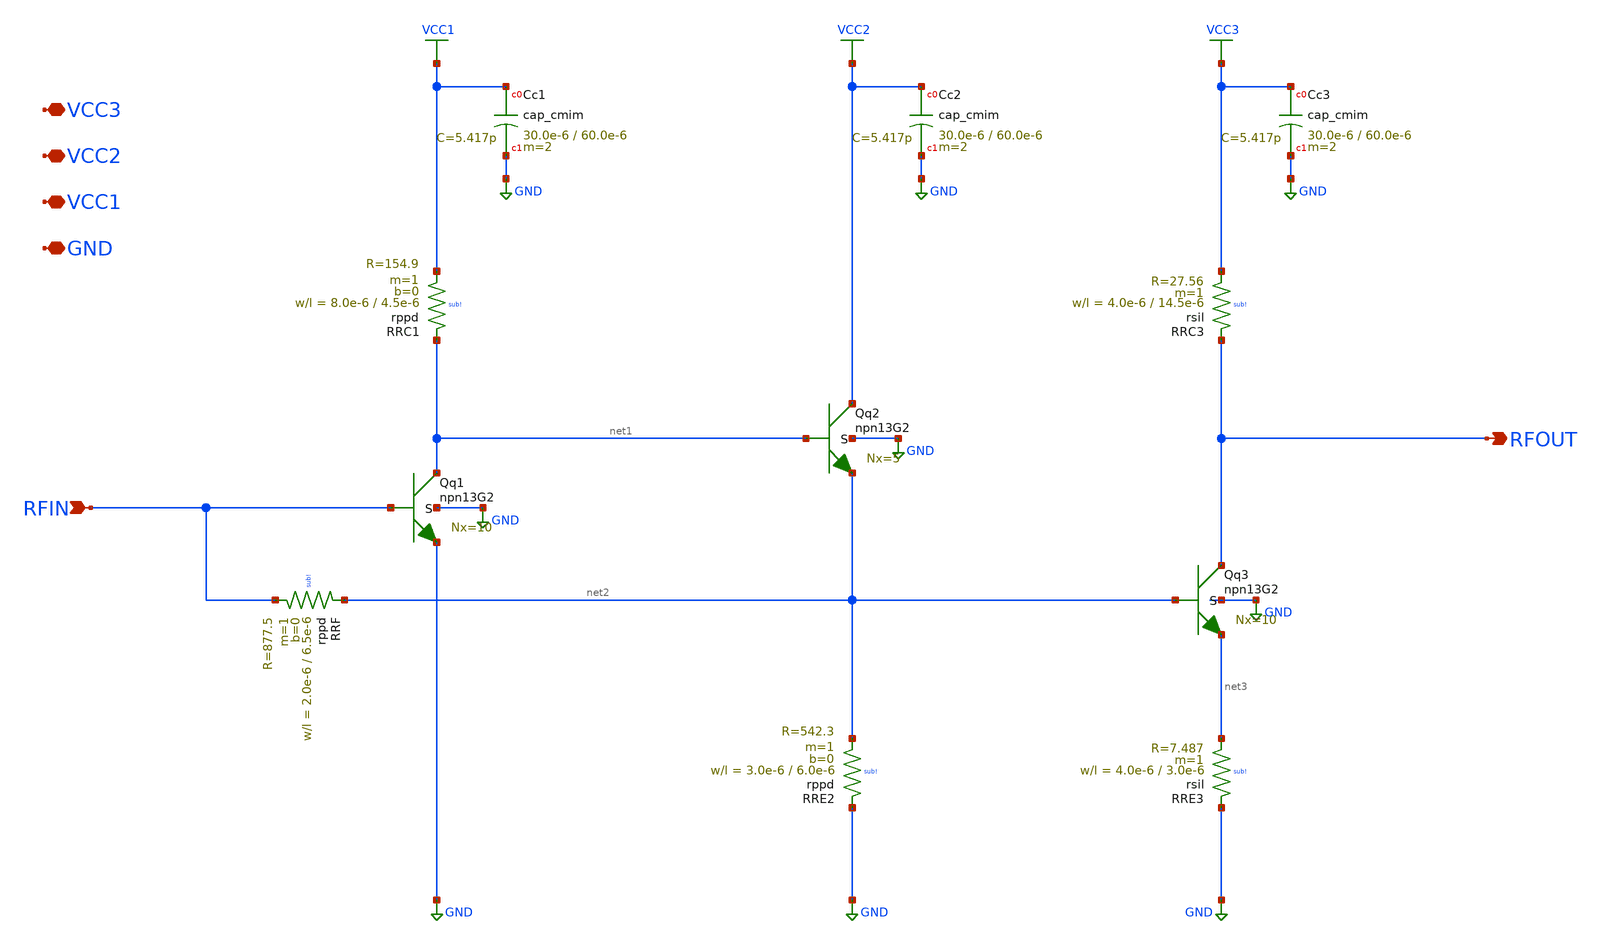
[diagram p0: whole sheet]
** sch_path: TO_Apr2025/40_GHZ_LOW_NOISE_TIA/xschem/40_GHZ_LOW_NOISE_TIA.sch
**.subckt 40_GHZ_LOW_NOISE_TIA RFIN GND VCC1 VCC2 RFOUT VCC3
*.ipin RFIN
*.iopin GND
*.iopin VCC1
*.iopin VCC2
*.opin RFOUT
*.iopin VCC3
XQq1 net1 RFIN GND GND npn13G2 Nx=10 mm_ok=1
XCc1 VCC1 GND cap_cmim w=30.0e-6 l=60.0e-6 m=2 mm_ok=1
XQq2 VCC2 net1 net2 GND npn13G2 Nx=5 mm_ok=1
XCc2 VCC2 GND cap_cmim w=30.0e-6 l=60.0e-6 m=2 mm_ok=1
XRRE2 GND net2 sub! rppd w=3.0e-6 l=6.0e-6 m=1 b=0 mm_ok=1
XRRC1 net1 VCC1 sub! rppd w=8.0e-6 l=4.5e-6 m=1 b=0 mm_ok=1
XQq3 RFOUT net2 net3 GND npn13G2 Nx=10 mm_ok=1
XRRF net2 RFIN sub! rppd w=2.0e-6 l=6.5e-6 m=1 b=0 mm_ok=1
XRRE3 GND net3 sub! rsil w=4.0e-6 l=3.0e-6 m=1 mm_ok=1
XRRC3 RFOUT VCC3 sub! rsil w=4.0e-6 l=14.5e-6 m=1 mm_ok=1
XCc3 VCC3 GND cap_cmim w=30.0e-6 l=60.0e-6 m=2 mm_ok=1
**.ends
.end
